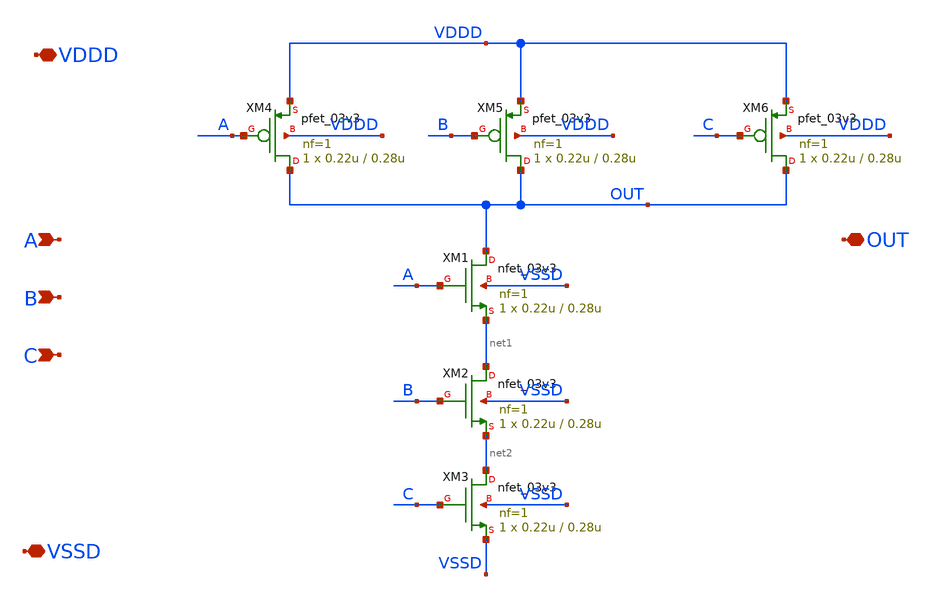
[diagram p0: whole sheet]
** sch_path: SAR_ADC/SAR_logic/xschem/nand_3_1x.sch
**.subckt nand_3_1x A B C VDDD VSSD OUT
*.ipin A
*.ipin B
*.ipin C
*.iopin VDDD
*.iopin VSSD
*.iopin OUT
XM1 OUT A net1 VSSD nfet_03v3 L=0.28u W=0.22u nf=1 ad='int((nf+1)/2) * W/nf * 0.18u' as='int((nf+2)/2) * W/nf * 0.18u'
+ pd='2*int((nf+1)/2) * (W/nf + 0.18u)' ps='2*int((nf+2)/2) * (W/nf + 0.18u)' nrd='0.18u / W' nrs='0.18u / W'
+ sa=0 sb=0 sd=0 m=1
XM2 net1 B net2 VSSD nfet_03v3 L=0.28u W=0.22u nf=1 ad='int((nf+1)/2) * W/nf * 0.18u' as='int((nf+2)/2) * W/nf * 0.18u'
+ pd='2*int((nf+1)/2) * (W/nf + 0.18u)' ps='2*int((nf+2)/2) * (W/nf + 0.18u)' nrd='0.18u / W' nrs='0.18u / W'
+ sa=0 sb=0 sd=0 m=1
XM3 net2 C VSSD VSSD nfet_03v3 L=0.28u W=0.22u nf=1 ad='int((nf+1)/2) * W/nf * 0.18u' as='int((nf+2)/2) * W/nf * 0.18u'
+ pd='2*int((nf+1)/2) * (W/nf + 0.18u)' ps='2*int((nf+2)/2) * (W/nf + 0.18u)' nrd='0.18u / W' nrs='0.18u / W'
+ sa=0 sb=0 sd=0 m=1
XM4 OUT A VDDD VDDD pfet_03v3 L=0.28u W=0.22u nf=1 ad='int((nf+1)/2) * W/nf * 0.18u' as='int((nf+2)/2) * W/nf * 0.18u'
+ pd='2*int((nf+1)/2) * (W/nf + 0.18u)' ps='2*int((nf+2)/2) * (W/nf + 0.18u)' nrd='0.18u / W' nrs='0.18u / W'
+ sa=0 sb=0 sd=0 m=1
XM5 OUT B VDDD VDDD pfet_03v3 L=0.28u W=0.22u nf=1 ad='int((nf+1)/2) * W/nf * 0.18u' as='int((nf+2)/2) * W/nf * 0.18u'
+ pd='2*int((nf+1)/2) * (W/nf + 0.18u)' ps='2*int((nf+2)/2) * (W/nf + 0.18u)' nrd='0.18u / W' nrs='0.18u / W'
+ sa=0 sb=0 sd=0 m=1
XM6 OUT C VDDD VDDD pfet_03v3 L=0.28u W=0.22u nf=1 ad='int((nf+1)/2) * W/nf * 0.18u' as='int((nf+2)/2) * W/nf * 0.18u'
+ pd='2*int((nf+1)/2) * (W/nf + 0.18u)' ps='2*int((nf+2)/2) * (W/nf + 0.18u)' nrd='0.18u / W' nrs='0.18u / W'
+ sa=0 sb=0 sd=0 m=1
**.ends
.end
